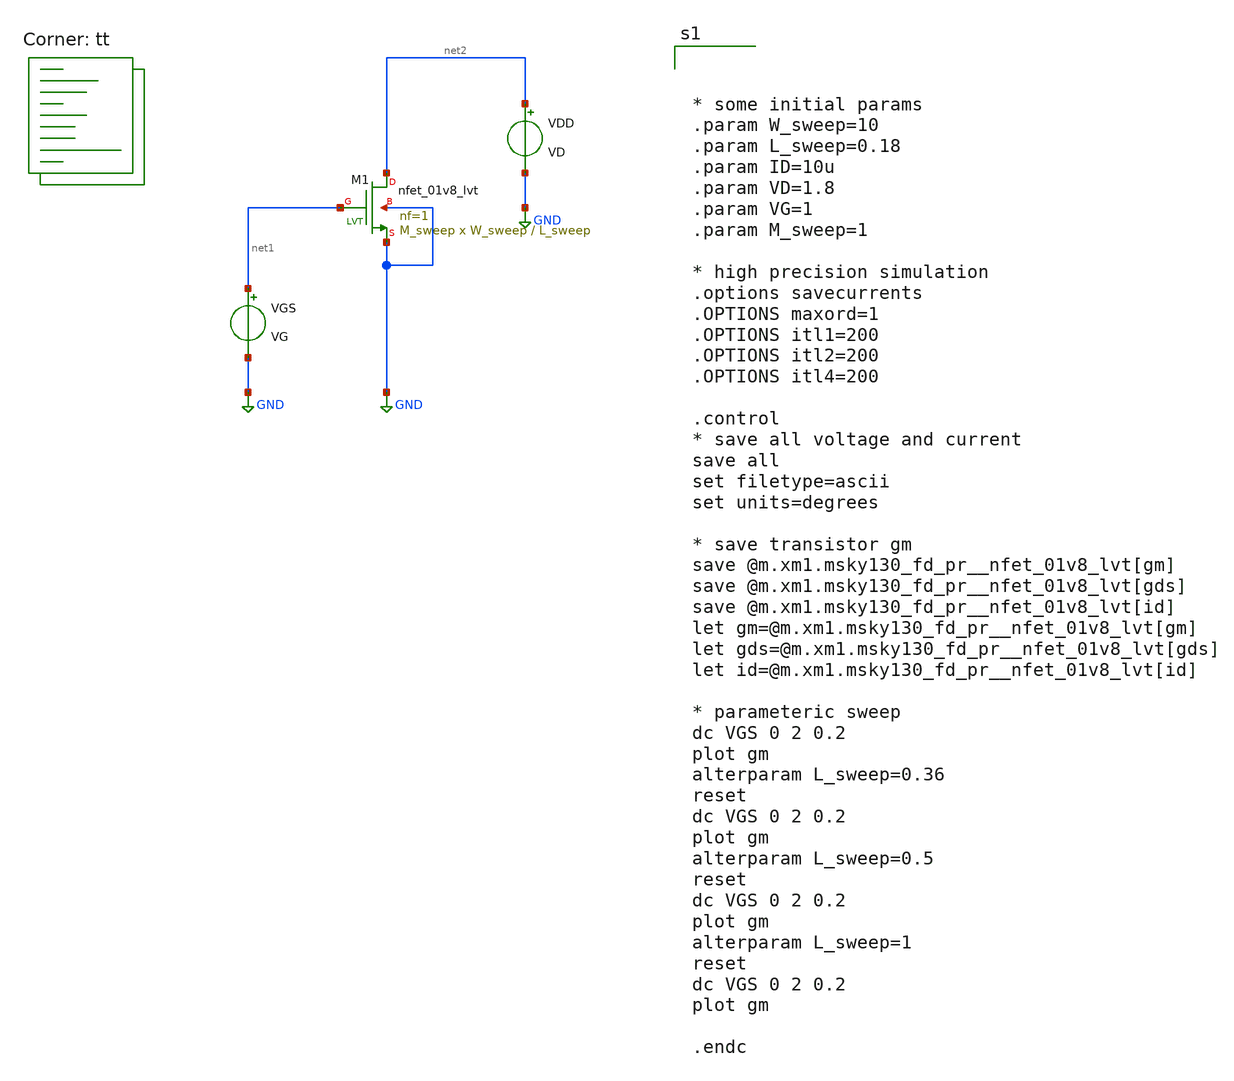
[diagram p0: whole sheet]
** sch_path: xschem/test_gm_id.sch
**.subckt test_gm_id
VDD net2 GND VD
VGS net1 GND VG
XM1 net2 net1 GND GND sky130_fd_pr__nfet_01v8_lvt L=L_sweep W=W_sweep nf=1 ad='int((nf+1)/2) * W/nf * 0.29'
+ as='int((nf+2)/2) * W/nf * 0.29' pd='2*int((nf+1)/2) * (W/nf + 0.29)' ps='2*int((nf+2)/2) * (W/nf + 0.29)'
+ nrd='0.29 / W' nrs='0.29 / W' sa=0 sb=0 sd=0 mult=M_sweep m=M_sweep
**** begin user architecture code
.lib $::SKYWATER_MODELS/sky130.lib.spice tt



* some initial params
.param W_sweep=10
.param L_sweep=0.18
.param ID=10u
.param VD=1.8
.param VG=1
.param M_sweep=1

* high precision simulation
.options savecurrents
.OPTIONS maxord=1
.OPTIONS itl1=200
.OPTIONS itl2=200
.OPTIONS itl4=200

.control
* save all voltage and current
save all
set filetype=ascii
set units=degrees

* save transistor gm
save @m.xm1.msky130_fd_pr__nfet_01v8_lvt[gm]
save @m.xm1.msky130_fd_pr__nfet_01v8_lvt[gds]
save @m.xm1.msky130_fd_pr__nfet_01v8_lvt[id]
let gm=@m.xm1.msky130_fd_pr__nfet_01v8_lvt[gm]
let gds=@m.xm1.msky130_fd_pr__nfet_01v8_lvt[gds]
let id=@m.xm1.msky130_fd_pr__nfet_01v8_lvt[id]

* parameteric sweep
dc VGS 0 2 0.2
plot gm
alterparam L_sweep=0.36
reset
dc VGS 0 2 0.2
plot gm
alterparam L_sweep=0.5
reset
dc VGS 0 2 0.2
plot gm
alterparam L_sweep=1
reset
dc VGS 0 2 0.2
plot gm

.endc


**** end user architecture code
**.ends
.GLOBAL GND
.end
